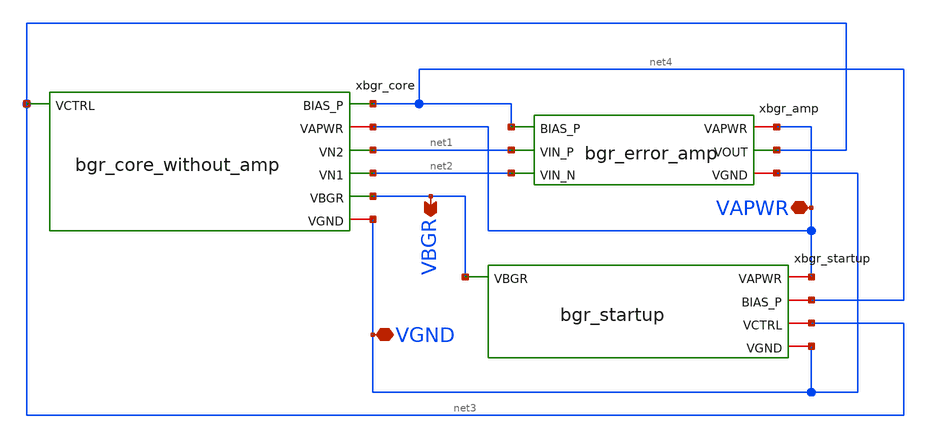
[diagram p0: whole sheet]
** sch_path: xschem/bgr.sch
**.subckt bgr VAPWR VGND VBGR
*.iopin VAPWR
*.iopin VGND
*.opin VBGR
xbgr_core net4 VAPWR net3 net1 net2 VBGR VGND bgr_core_without_amp
xbgr_amp net4 VAPWR net1 net2 net3 VGND bgr_error_amp
xbgr_startup VAPWR VBGR net4 net3 VGND bgr_startup
**.ends

* expanding   symbol:  bgr_core_without_amp.sym # of pins=7
** sym_path: xschem/bgr_core_without_amp.sym
** sch_path: xschem/bgr_core_without_amp.sch
.subckt bgr_core_without_amp BIAS_P VAPWR VCTRL VN2 VN1 VBGR VGND
*.iopin VGND
*.iopin VAPWR
*.opin VBGR
*.ipin VCTRL
*.opin BIAS_P
*.opin VN1
*.opin VN2
XQ1 VN1 VBGR E1 VGND npn_05p00x05p00 m=1
XQ2 VN2 VBGR E2 VGND npn_05p00x05p00 m=8
XR1 E1 E2 VGND ppolyf_u_1k r_width=1.18e-6 r_length=3e-6 m=1
XR2 VGND E1 VGND ppolyf_u_1k r_width=1e-6 r_length=62.65e-6 m=1
XR3 VGND VBGR VGND ppolyf_u_1k r_width=1e-6 r_length=137e-6 m=1
XM1 VN2 VCTRL VAPWR VAPWR pfet_03v3 L=4u W=8u nf=1 ad='int((nf+1)/2) * W/nf * 0.18u' as='int((nf+2)/2) * W/nf * 0.18u'
+ pd='2*int((nf+1)/2) * (W/nf + 0.18u)' ps='2*int((nf+2)/2) * (W/nf + 0.18u)' nrd='0.18u / W' nrs='0.18u / W'
+ sa=0 sb=0 sd=0 m=1
XM2 VN1 VCTRL VAPWR VAPWR pfet_03v3 L=4u W=8u nf=1 ad='int((nf+1)/2) * W/nf * 0.18u' as='int((nf+2)/2) * W/nf * 0.18u'
+ pd='2*int((nf+1)/2) * (W/nf + 0.18u)' ps='2*int((nf+2)/2) * (W/nf + 0.18u)' nrd='0.18u / W' nrs='0.18u / W'
+ sa=0 sb=0 sd=0 m=1
XM3 NBIAS_N VCTRL VAPWR VAPWR pfet_03v3 L=4u W=2u nf=1 ad='int((nf+1)/2) * W/nf * 0.18u' as='int((nf+2)/2) * W/nf * 0.18u'
+ pd='2*int((nf+1)/2) * (W/nf + 0.18u)' ps='2*int((nf+2)/2) * (W/nf + 0.18u)' nrd='0.18u / W' nrs='0.18u / W'
+ sa=0 sb=0 sd=0 m=1
XM4 VBGR VCTRL VAPWR VAPWR pfet_03v3 L=4u W=64u nf=1 ad='int((nf+1)/2) * W/nf * 0.18u' as='int((nf+2)/2) * W/nf * 0.18u'
+ pd='2*int((nf+1)/2) * (W/nf + 0.18u)' ps='2*int((nf+2)/2) * (W/nf + 0.18u)' nrd='0.18u / W' nrs='0.18u / W'
+ sa=0 sb=0 sd=0 m=1
XM5 BIAS_P BIAS_P VAPWR VAPWR pfet_03v3 L=4u W=1u nf=1 ad='int((nf+1)/2) * W/nf * 0.18u' as='int((nf+2)/2) * W/nf * 0.18u'
+ pd='2*int((nf+1)/2) * (W/nf + 0.18u)' ps='2*int((nf+2)/2) * (W/nf + 0.18u)' nrd='0.18u / W' nrs='0.18u / W'
+ sa=0 sb=0 sd=0 m=1
XM6 BIAS_P NBIAS_N VGND VGND nfet_03v3 L=4u W=1u nf=1 ad='int((nf+1)/2) * W/nf * 0.18u' as='int((nf+2)/2) * W/nf * 0.18u'
+ pd='2*int((nf+1)/2) * (W/nf + 0.18u)' ps='2*int((nf+2)/2) * (W/nf + 0.18u)' nrd='0.18u / W' nrs='0.18u / W'
+ sa=0 sb=0 sd=0 m=1
XM7 NBIAS_N NBIAS_N VGND VGND nfet_03v3 L=4u W=1u nf=1 ad='int((nf+1)/2) * W/nf * 0.18u' as='int((nf+2)/2) * W/nf * 0.18u'
+ pd='2*int((nf+1)/2) * (W/nf + 0.18u)' ps='2*int((nf+2)/2) * (W/nf + 0.18u)' nrd='0.18u / W' nrs='0.18u / W'
+ sa=0 sb=0 sd=0 m=1
.ends


* expanding   symbol:  bgr_error_amp.sym # of pins=6
** sym_path: xschem/bgr_error_amp.sym
** sch_path: xschem/bgr_error_amp.sch
.subckt bgr_error_amp BIAS_P VAPWR VIN_P VIN_N VOUT VGND
*.ipin VIN_P
*.ipin VIN_N
*.ipin BIAS_P
*.iopin VAPWR
*.iopin VGND
*.opin VOUT
XMDIFF_P net1 VIN_P TAIL_P VAPWR pfet_03v3 L=0.28u W=0.22u nf=1 ad='int((nf+1)/2) * W/nf * 0.18u' as='int((nf+2)/2) * W/nf * 0.18u'
+ pd='2*int((nf+1)/2) * (W/nf + 0.18u)' ps='2*int((nf+2)/2) * (W/nf + 0.18u)' nrd='0.18u / W' nrs='0.18u / W'
+ sa=0 sb=0 sd=0 m=1
XMDIFF_N VOUT VIN_N TAIL_P VAPWR pfet_03v3 L=0.28u W=0.22u nf=1 ad='int((nf+1)/2) * W/nf * 0.18u' as='int((nf+2)/2) * W/nf * 0.18u'
+ pd='2*int((nf+1)/2) * (W/nf + 0.18u)' ps='2*int((nf+2)/2) * (W/nf + 0.18u)' nrd='0.18u / W' nrs='0.18u / W'
+ sa=0 sb=0 sd=0 m=1
XMTAIL TAIL_P BIAS_P VAPWR VAPWR pfet_03v3 L=0.28u W=0.22u nf=1 ad='int((nf+1)/2) * W/nf * 0.18u' as='int((nf+2)/2) * W/nf * 0.18u'
+ pd='2*int((nf+1)/2) * (W/nf + 0.18u)' ps='2*int((nf+2)/2) * (W/nf + 0.18u)' nrd='0.18u / W' nrs='0.18u / W'
+ sa=0 sb=0 sd=0 m=1
XMLOAD_REF net1 net1 VGND VGND nfet_03v3 L=0.28u W=0.22u nf=1 ad='int((nf+1)/2) * W/nf * 0.18u' as='int((nf+2)/2) * W/nf * 0.18u'
+ pd='2*int((nf+1)/2) * (W/nf + 0.18u)' ps='2*int((nf+2)/2) * (W/nf + 0.18u)' nrd='0.18u / W' nrs='0.18u / W'
+ sa=0 sb=0 sd=0 m=1
XMLOAD_OUT VOUT net1 VGND VGND nfet_03v3 L=0.28u W=0.22u nf=1 ad='int((nf+1)/2) * W/nf * 0.18u' as='int((nf+2)/2) * W/nf * 0.18u'
+ pd='2*int((nf+1)/2) * (W/nf + 0.18u)' ps='2*int((nf+2)/2) * (W/nf + 0.18u)' nrd='0.18u / W' nrs='0.18u / W'
+ sa=0 sb=0 sd=0 m=1
.ends


* expanding   symbol:  bgr_startup.sym # of pins=5
** sym_path: xschem/bgr_startup.sym
** sch_path: xschem/bgr_startup.sch
.subckt bgr_startup VAPWR VBGR BIAS_P VCTRL VGND
*.iopin VAPWR
*.iopin VGND
*.ipin VBGR
*.iopin BIAS_P
*.iopin VCTRL
XM1 START_ON VBGR VGND VGND nfet_03v3 L=0.28u W=0.22u nf=1 ad='int((nf+1)/2) * W/nf * 0.18u' as='int((nf+2)/2) * W/nf * 0.18u'
+ pd='2*int((nf+1)/2) * (W/nf + 0.18u)' ps='2*int((nf+2)/2) * (W/nf + 0.18u)' nrd='0.18u / W' nrs='0.18u / W'
+ sa=0 sb=0 sd=0 m=1
XM2 BIAS_P START_ON VGND VGND nfet_03v3 L=0.28u W=0.22u nf=1 ad='int((nf+1)/2) * W/nf * 0.18u' as='int((nf+2)/2) * W/nf * 0.18u'
+ pd='2*int((nf+1)/2) * (W/nf + 0.18u)' ps='2*int((nf+2)/2) * (W/nf + 0.18u)' nrd='0.18u / W' nrs='0.18u / W'
+ sa=0 sb=0 sd=0 m=1
XM3 VCTRL START_ON VGND VGND nfet_03v3 L=0.28u W=0.22u nf=1 ad='int((nf+1)/2) * W/nf * 0.18u' as='int((nf+2)/2) * W/nf * 0.18u'
+ pd='2*int((nf+1)/2) * (W/nf + 0.18u)' ps='2*int((nf+2)/2) * (W/nf + 0.18u)' nrd='0.18u / W' nrs='0.18u / W'
+ sa=0 sb=0 sd=0 m=1
XM4 START_ON VBGR VAPWR VAPWR pfet_03v3 L=0.28u W=0.22u nf=1 ad='int((nf+1)/2) * W/nf * 0.18u' as='int((nf+2)/2) * W/nf * 0.18u'
+ pd='2*int((nf+1)/2) * (W/nf + 0.18u)' ps='2*int((nf+2)/2) * (W/nf + 0.18u)' nrd='0.18u / W' nrs='0.18u / W'
+ sa=0 sb=0 sd=0 m=1
.ends

.end
